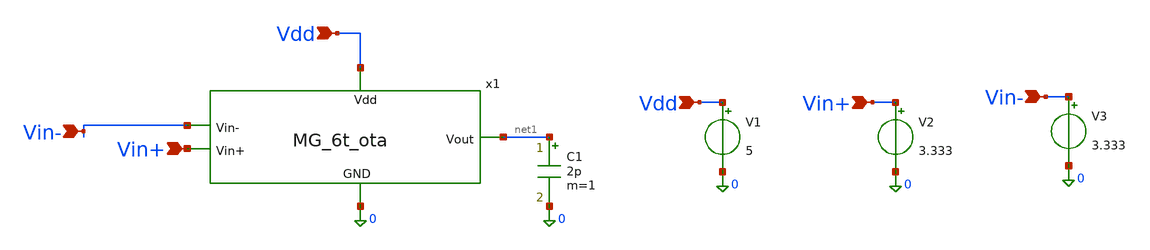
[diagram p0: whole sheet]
** sch_path: MG_6T_OTA/MG_6t_ota_testbench.sch
**.subckt MG_6t_ota_testbench Vdd Vin+ Vin- Vdd Vin+ Vin-
*.ipin Vdd
*.ipin Vin+
*.ipin Vin-
*.ipin Vdd
*.ipin Vin+
*.ipin Vin-
V1 Vdd 0 5
V2 Vin+ 0 3.333
V3 Vin- 0 3.333
C1 net1 0 2p m=1
x1 Vdd net1 Vin- Vin+ 0 MG_6t_ota
**** begin user architecture code


.include /foss/pdks/gf180mcuD/libs.tech/ngspice/design.ngspice
.lib /foss/pdks/gf180mcuD/libs.tech/ngspice/sm141064.ngspice typical
.lib /foss/pdks/gf180mcuD/libs.tech/ngspice/sm141064.ngspice res_typical
.op

**** end user architecture code
**.ends
.end
